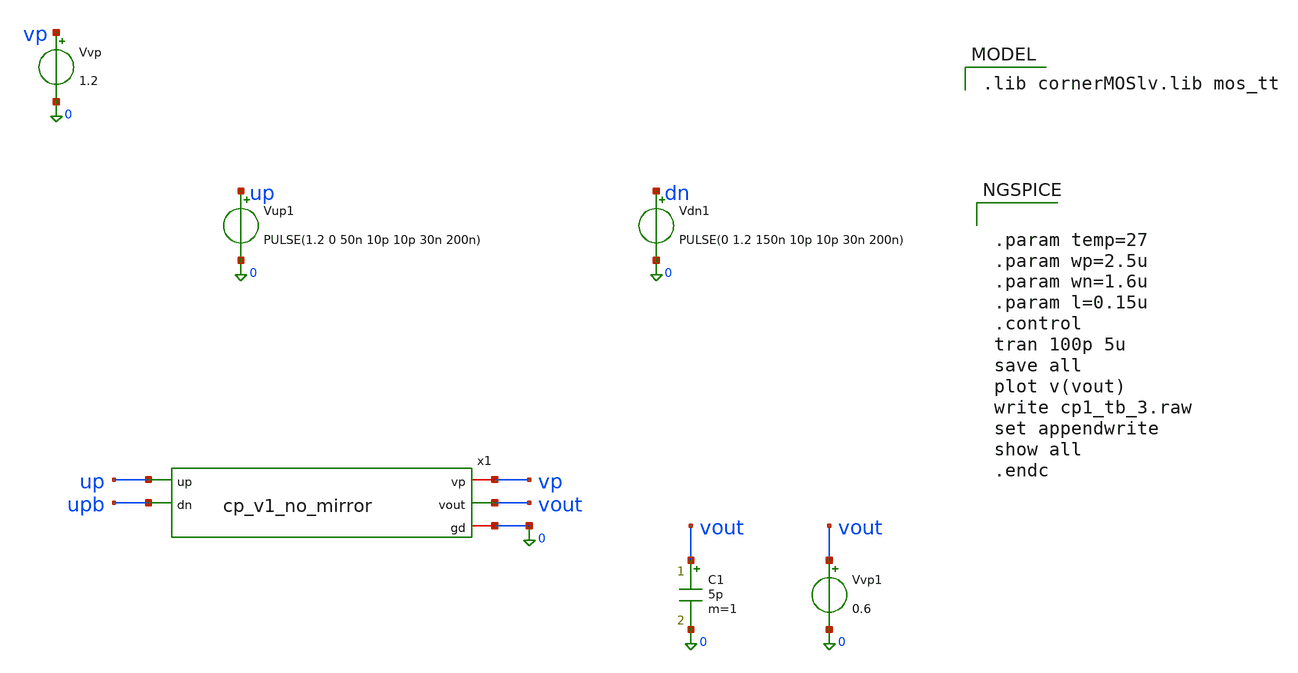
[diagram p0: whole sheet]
** sch_path: PLL0663-main/schematic/xschem/charge_pump/old_sch/cp_v1_tb.sch
**.subckt cp_v1_tb
Vvp vp 0 1.2
Vup1 up 0 PULSE(1.2 0 50n 10p 10p 30n 200n)
Vdn1 dn 0 PULSE(0 1.2 150n 10p 10p 30n 200n)
C1 vout 0 5p m=1
x1 vp up vout upb 0 cp_v1_no_mirror
Vvp1 vout 0 0.6
**** begin user architecture code
 .lib cornerMOSlv.lib mos_tt



.param temp=27
.param wp=2.5u
.param wn=1.6u
.param l=0.15u
.control
tran 100p 5u
save all
plot v(vout)
write cp1_tb_3.raw
set appendwrite
show all
.endc


**** end user architecture code
**.ends
.end
